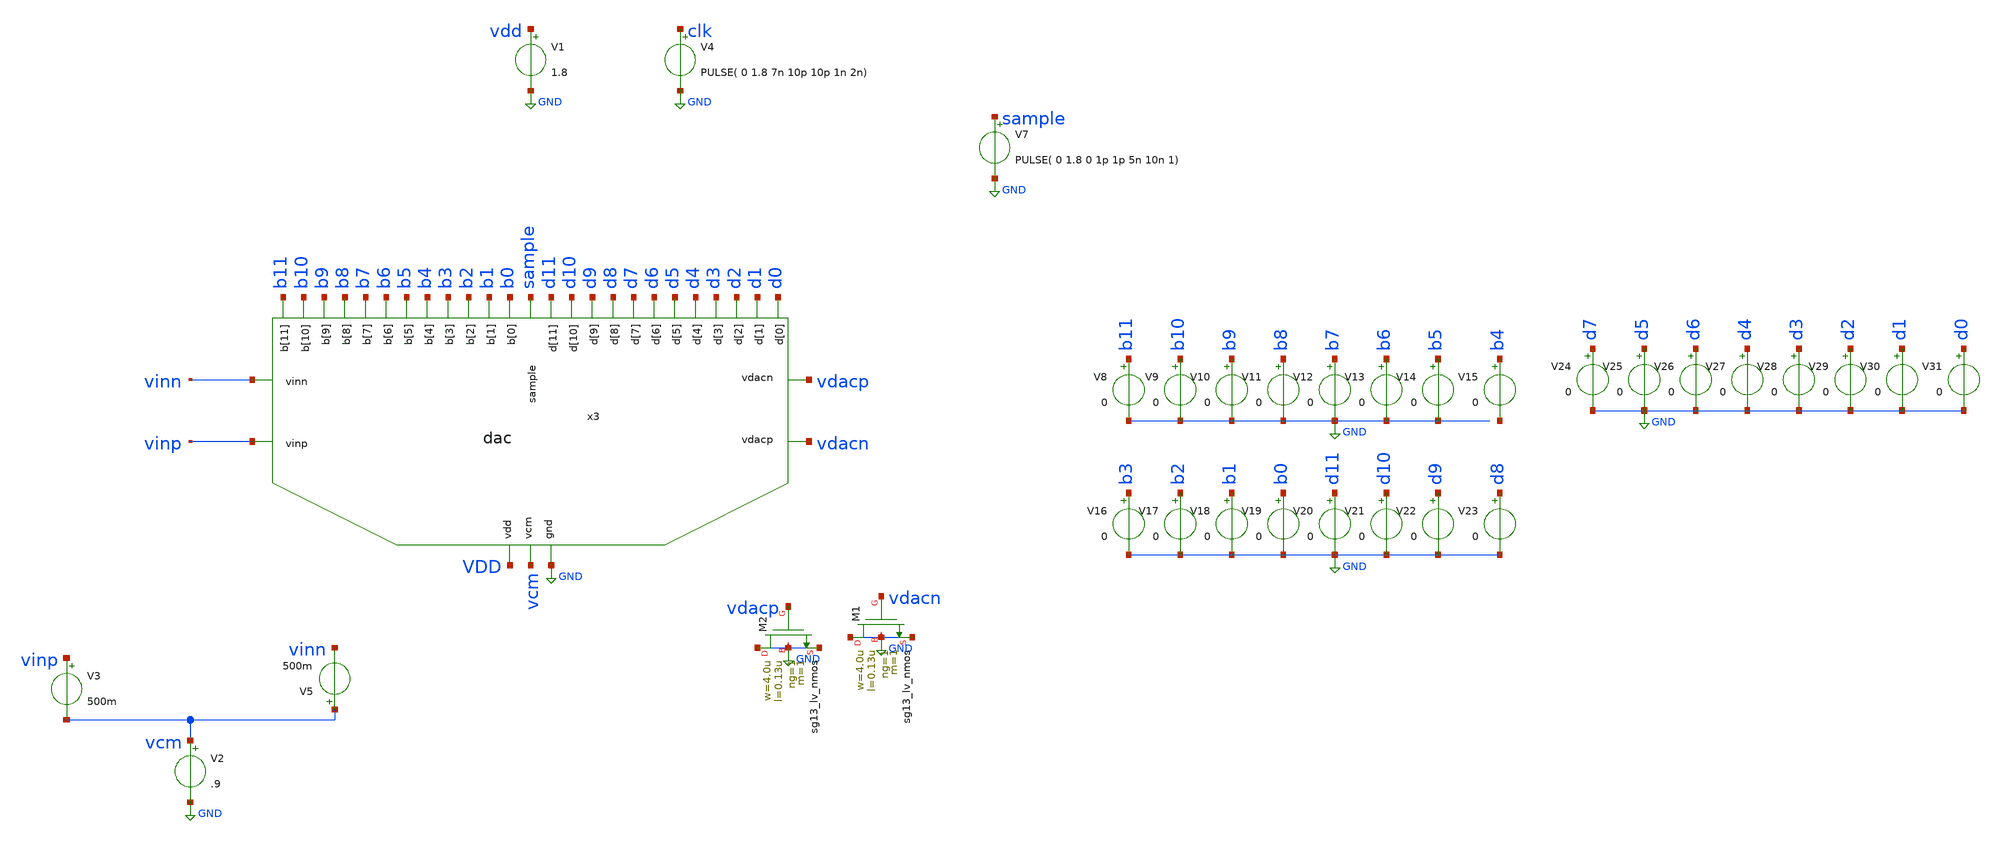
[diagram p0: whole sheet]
** sch_path: xschem/dac_icms_cell_ideall/testbenches/tb_dac_only.sch
* IHP-GmbH/IHP-Open-PDK/ihp-sg13g2/libs.tech/xschem/sg13g2_stdcells/sg13g2_inv_2.sch:
* Copyright 2023 IHP PDK Authors
* Licensed under the Apache License, Version 2.0 (the "License");
**.subckt tb_dac_only
x3 vdacp vcm b9 b7 b0 b11 b3 b4 b2 b1 b8 b6 b5 b10 GND VDD sample vdacn vinp vinn d9 d7 d0 d11 d3 d4
+ d2 d1 d8 d6 d5 d10 dac cu=100f
V1 vdd GND 1.8
V2 vcm GND .9
V3 vinp vcm 500m
V4 clk GND PULSE( 0 1.8 7n 10p 10p 1n 2n)
V7 sample GND PULSE( 0 1.8 0 1p 1p 5n 10n 1)
XM2 GND vdacp GND GND sg13_lv_nmos w=4.0u l=0.13u ng=1 m=1 mm_ok=1
XM1 GND vdacn GND GND sg13_lv_nmos w=4.0u l=0.13u ng=1 m=1 mm_ok=1
V8 b11 GND 0
V9 b10 GND 0
V10 b9 GND 0
V11 b8 GND 0
V12 b7 GND 0
V13 b6 GND 0
V14 b5 GND 0
V15 b4 net1 0
V16 b3 GND 0
V17 b2 GND 0
V18 b1 GND 0
V19 b0 GND 0
V20 d11 GND 0
V21 d10 GND 0
V22 d9 GND 0
V23 d8 GND 0
V24 d7 GND 0
V25 d5 GND 0
V26 d6 GND 0
V27 d4 GND 0
V28 d3 GND 0
V29 d2 GND 0
V30 d1 GND 0
V31 d0 GND 0
V5 vcm vinn 500m
**** begin user architecture code


.param temp=27
.param W_P = 1.0u
.param L_P = 0.13u
.param W_N = 1.0u
.param L_N = 0.13u
.options savecurrents klu method=gear reltol=1e-2 abstol=1e-15 gmin=1e-10
.control

* Transient Analysis
tran 100p 20n

*plot {d0} {d1 + 4} {d2 + 8} {d3 + 12} {d4 + 16} {d5 + 20} {d6 + 24} {d7 + 28} {d8 + 32} {d9 + 36} {d10 + 40}
*+ {d11 + 44}
*plot {b0} {b1 + 4} {b2 + 8} {b3 + 12} {b4 + 16} {b5 + 20} {b6 + 24} {b7 + 28} {b8 + 32} {b9 + 36} {b10 + 40}
*+ {b11 + 44}
*plot {clk} {comp_in + 2} {sample + 4}
plot vdacp vdacn sample
plot {vdacp-vdacn}
plot x3.x14.net1-vdacp x3.x18.vcap-vdacn

.endc




** IHP models
.lib cornerMOSlv.lib mos_tt
.lib cornerMOShv.lib mos_tt
.lib cornerHBT.lib hbt_typ
.lib cornerRES.lib res_typ
.include /foss/pdks/ihp-sg13g2/libs.ref/sg13g2_stdcell/spice/sg13g2_stdcell.spice


**** end user architecture code
**.ends

* expanding   symbol:  dac_icms_cell/dac.sym # of pins=32
** sym_path: xschem/dac_icms_cell_ideal/dac.sym
** sch_path: xschem/dac_icms_cell_ideal/dac.sch
.subckt dac vdacn vcm b9 b7 b0 b11 b3 b4 b2 b1 b8 b6 b5 b10 VSS VDD sample_pin vdacp vinp vinn D9 D7
+ D0 D11 D3 D4 D2 D1 D8 D6 D5 D10  cu=5u
*.ipin D0
*.ipin b0
*.iopin vinp
*.iopin vcm
*.ipin sample_pin
*.iopin vinn
*.iopin vdacp
*.iopin vdacn
*.iopin VSS
*.iopin VDD
*.ipin D1
*.ipin b1
*.ipin D2
*.ipin b2
*.ipin D3
*.ipin b3
*.ipin D4
*.ipin b4
*.ipin D5
*.ipin b5
*.ipin D6
*.ipin b6
*.ipin D7
*.ipin b7
*.ipin D8
*.ipin b8
*.ipin D9
*.ipin b9
*.ipin D10
*.ipin b10
*.ipin D11
*.ipin b11
x14 VDD D0 VSS vdacn b0 vcm vinn a_sample a_sample_n b_sample b_sample_n unit_cell_n W_P=
+ L_P_SPDT=0.13u W_N= L_N_SPDT=0.13u Cu=cu n=32
x18 VDD D0 VSS vdacp b0 vcm vinp a_sample a_sample_n b_sample b_sample_n unit_cell W_P_SPDT=1.0u
+ L_P_SPDT=0.13u W_N_SPDT=1.0u L_N_SPDT=0.13u Cu=cu n=32
C1 vdacp2 vdacn cu m=1
C4 vdacp2 vcm cu m=1
x1 VDD D1 VSS vdacn b1 vcm vinn a_sample a_sample_n b_sample b_sample_n unit_cell_n W_P=
+ L_P_SPDT=0.13u W_N= L_N_SPDT=0.13u Cu=cu n=16
x2 VDD D2 VSS vdacn b2 vcm vinn a_sample a_sample_n b_sample b_sample_n unit_cell_n W_P=
+ L_P_SPDT=0.13u W_N= L_N_SPDT=0.13u Cu=cu n=8
x3 VDD D3 VSS vdacn b3 vcm vinn a_sample a_sample_n b_sample b_sample_n unit_cell_n W_P=
+ L_P_SPDT=0.13u W_N= L_N_SPDT=0.13u Cu=cu n=4
x4 VDD D4 VSS vdacn b4 vcm vinn a_sample a_sample_n b_sample b_sample_n unit_cell_n W_P=
+ L_P_SPDT=0.13u W_N= L_N_SPDT=0.13u Cu=cu n=2
x5 VDD D5 VSS vdacn b5 vcm vinn a_sample a_sample_n b_sample b_sample_n unit_cell_n W_P=
+ L_P_SPDT=0.13u W_N= L_N_SPDT=0.13u Cu=cu n=1
x6 VDD D6 VSS vdacp2 b6 vcm vinn a_sample a_sample_n b_sample b_sample_n unit_cell_n W_P=
+ L_P_SPDT=0.13u W_N= L_N_SPDT=0.13u Cu=cu n=32
x7 VDD D7 VSS vdacp2 b7 vcm vinn a_sample a_sample_n b_sample b_sample_n unit_cell_n W_P=
+ L_P_SPDT=0.13u W_N= L_N_SPDT=0.13u Cu=cu n=16
x8 VDD D8 VSS vdacp2 b8 vcm vinn a_sample a_sample_n b_sample b_sample_n unit_cell_n W_P=
+ L_P_SPDT=0.13u W_N= L_N_SPDT=0.13u Cu=cu n=8
x9 VDD D9 VSS vdacp2 b9 vcm vinn a_sample a_sample_n b_sample b_sample_n unit_cell_n W_P=
+ L_P_SPDT=0.13u W_N= L_N_SPDT=0.13u Cu=cu n=4
x11 VDD D10 VSS vdacp2 b10 vcm vinn a_sample a_sample_n b_sample b_sample_n unit_cell_n W_P=
+ L_P_SPDT=0.13u W_N= L_N_SPDT=0.13u Cu=cu n=2
x12 VDD D11 VSS vdacp2 b11 vcm vinn a_sample a_sample_n b_sample b_sample_n unit_cell_n W_P=
+ L_P_SPDT=0.13u W_N= L_N_SPDT=0.13u Cu=cu n=1
x13 VDD D1 VSS vdacp b1 vcm vinp a_sample a_sample_n b_sample b_sample_n unit_cell W_P_SPDT=1.0u
+ L_P_SPDT=0.13u W_N_SPDT=1.0u L_N_SPDT=0.13u Cu=cu n=16
x15 VDD D2 VSS vdacp b2 vcm vinp a_sample a_sample_n b_sample b_sample_n unit_cell W_P_SPDT=1.0u
+ L_P_SPDT=0.13u W_N_SPDT=1.0u L_N_SPDT=0.13u Cu=cu n=8
x16 VDD D3 VSS vdacp b3 vcm vinp a_sample a_sample_n b_sample b_sample_n unit_cell W_P_SPDT=1.0u
+ L_P_SPDT=0.13u W_N_SPDT=1.0u L_N_SPDT=0.13u Cu=cu n=4
x19 VDD D4 VSS vdacp b4 vcm vinp a_sample a_sample_n b_sample b_sample_n unit_cell W_P_SPDT=1.0u
+ L_P_SPDT=0.13u W_N_SPDT=1.0u L_N_SPDT=0.13u Cu=cu n=2
x20 VDD D5 VSS vdacp b5 vcm vinp a_sample a_sample_n b_sample b_sample_n unit_cell W_P_SPDT=1.0u
+ L_P_SPDT=0.13u W_N_SPDT=1.0u L_N_SPDT=0.13u Cu=cu n=32
C3 vdacn2 vdacp cu m=1
x21 VDD D6 VSS vdacn2 b6 vcm vinp a_sample a_sample_n b_sample b_sample_n unit_cell W_P_SPDT=1.0u
+ L_P_SPDT=0.13u W_N_SPDT=1.0u L_N_SPDT=0.13u Cu=cu n=32
x22 VDD D7 VSS vdacn2 b7 vcm vinp a_sample a_sample_n b_sample b_sample_n unit_cell W_P_SPDT=1.0u
+ L_P_SPDT=0.13u W_N_SPDT=1.0u L_N_SPDT=0.13u Cu=cu n=16
x23 VDD D8 VSS vdacn2 b8 vcm vinp a_sample a_sample_n b_sample b_sample_n unit_cell W_P_SPDT=1.0u
+ L_P_SPDT=0.13u W_N_SPDT=1.0u L_N_SPDT=0.13u Cu=cu n=8
x24 VDD D9 VSS vdacn2 b9 vcm vinp a_sample a_sample_n b_sample b_sample_n unit_cell W_P_SPDT=1.0u
+ L_P_SPDT=0.13u W_N_SPDT=1.0u L_N_SPDT=0.13u Cu=cu n=4
x25 VDD D10 VSS vdacn2 b10 vcm vinp a_sample a_sample_n b_sample b_sample_n unit_cell W_P_SPDT=1.0u
+ L_P_SPDT=0.13u W_N_SPDT=1.0u L_N_SPDT=0.13u Cu=cu n=2
x26 VDD D11 VSS vdacn2 b11 vcm vinp a_sample a_sample_n b_sample b_sample_n unit_cell W_P_SPDT=1.0u
+ L_P_SPDT=0.13u W_N_SPDT=1.0u L_N_SPDT=0.13u Cu=cu n=32
C5 vcm vdacn2 cu m=1
x27 VDD b_n_ctrl net3 VSS inverter_lv W_P=1.0u L_P=0.13u W_N=1.0u L_N=0.13u N_C=1
x28 VDD net3 b_sample_n VSS inverter_lv W_P=10.0u L_P=0.13u W_N=10.0u L_N=0.13u N_C=1
x29 VDD b_ctrl net4 VSS inverter_lv W_P=1.0u L_P=0.13u W_N=1.0u L_N=0.13u N_C=1
x31 VDD net4 b_sample VSS inverter_lv W_P=10.0u L_P=0.13u W_N=10.0u L_N=0.13u N_C=1
x32 VDD a_n_ctrl net5 VSS inverter_lv W_P=1.0u L_P=0.13u W_N=1.0u L_N=0.13u N_C=1
x33 VDD net5 a_sample_n VSS inverter_lv W_P=20.0u L_P=0.13u W_N=10.0u L_N=0.13u N_C=1
x35 VDD a_ctrl net6 VSS inverter_lv W_P=1.0u L_P=0.13u W_N=1.0u L_N=0.13u N_C=1
x36 VDD net6 a_sample VSS inverter_lv W_P=20.0u L_P=0.13u W_N=10.0u L_N=0.13u N_C=1
x38 b_ctrl sample_pin net2 VDD VSS sg13g2_nor2_2
x39 a_n_ctrl net1 sample_pin VDD VSS sg13g2_nand2_2
x40 b_n_ctrl b_ctrl VDD VSS sg13g2_inv_2
x41 a_ctrl a_n_ctrl VDD VSS sg13g2_inv_2
x42 net2 a_sample_n net7 VDD VSS sg13g2_nand2_2
x43 net1 b_sample net8 VDD VSS sg13g2_nor2_2
x44 net7 a_sample VDD VSS sg13g2_inv_1
x45 net8 b_sample_n VDD VSS sg13g2_inv_1
.ends


* expanding   symbol:  dac_icms_cell/unit_cell_n.sym # of pins=11
** sym_path: xschem/dac_icms_cell/unit_cell_n.sym
** sch_path: xschem/dac_icms_cell/unit_cell_n.sch
.subckt unit_cell_n VDD d VSS v_top bit v_cm v_in a_sample a_sample_n b_sample b_sample_n
+  W_P_SPDT=1.0u L_P_SPDT=0.13u W_N_SPDT=1.0u L_N_SPDT=0.13u Cu=8f n=1
*.iopin VSS
*.iopin v_in
*.iopin VDD
*.ipin d
*.ipin bit
*.iopin v_top
*.iopin v_cm
*.ipin a_sample
*.ipin a_sample_n
*.ipin b_sample
*.ipin b_sample_n
x1 VDD d VSS net1 bit v_cm v_in b_sample_n b_sample dac_switch_n W_P_TG=3.0u L_P_TG=0.13u
+ W_N_TG=1.0u L_N_TG=0.13u n=n
C1 net1 v_top Cu m=n
x2 VDD a_sample VSS v_cm v_top a_sample_n transmission_gate_lv_w_dummy W_P=W_P_SPDT L_P=L_P_SPDT
+ W_N=W_N_SPDT L_N=L_N_SPDT W_P_D=1.0u L_P_D=0.13u W_N_D=1.0u L_N_D=0.13u n=n
.ends


* expanding   symbol:  dac_icms_cell/unit_cell.sym # of pins=11
** sym_path: xschem/dac_icms_cell/unit_cell.sym
** sch_path: xschem/dac_icms_cell/unit_cell.sch
.subckt unit_cell VDD d VSS v_top bit v_cm v_in a_sample a_sample_n b_sample b_sample_n
+  W_P_SPDT=1.0u L_P_SPDT=0.13u W_N_SPDT=1.0u L_N_SPDT=0.13u Cu=8f n=1
*.iopin VSS
*.iopin v_in
*.iopin VDD
*.ipin d
*.ipin bit
*.iopin v_top
*.iopin v_cm
*.ipin a_sample_n
*.ipin a_sample
*.ipin b_sample
*.ipin b_sample_n
x1 VDD d VSS net1 bit v_cm v_in b_sample_n b_sample dac_switch W_P=W_P_SPDT L_P_TG=0.13u
+ W_N=W_N_SPDT L_N_TG=0.13u n=n
C1 net1 v_top Cu m=n
x2 VDD a_sample_n VSS v_cm v_top a_sample transmission_gate_lv_w_dummy W_P=W_P_SPDT L_P=L_P_SPDT
+ W_N=W_N_SPDT L_N=L_N_SPDT W_P_D=1.0u L_P_D=0.13u W_N_D=1.0u L_N_D=0.13u n=n
.ends


* expanding   symbol:  inverter/inverter_lv.sym # of pins=4
** sym_path: xschem/inverter/inverter_lv.sym
** sch_path: xschem/inverter/inverter_lv.sch
.subckt inverter_lv VDD vin vout VSS  W_P=3.0u L_P=0.13u W_N=1.0u L_N=0.13u N_C=1
*.ipin vin
*.iopin VDD
*.iopin VSS
*.opin vout
XM1 vout vin VDD VDD sg13_lv_pmos w=W_P l=L_P ng=1 m={N_C} mm_ok=1
XM2 vout vin VSS VSS sg13_lv_nmos w=W_N l=L_N ng=1 m={N_C} mm_ok=1
.ends


* expanding   symbol:  sg13g2_stdcells/sg13g2_nor2_2.sym # of pins=3
** sym_path: sg13g2_stdcells/sg13g2_nor2_2.sym
** sch_path: sg13g2_stdcells/sg13g2_nor2_2.sch
.subckt sg13g2_nor2_2 Y A B VDD VSS
*.opin Y
*.ipin B
*.ipin A
*.iopin VDD
*.iopin VSS
XM1 Y A VSS VSS sg13_lv_nmos w=1.48u l=130.00n ng=2 m=1 mm_ok=1
XM2 Y B VSS VSS sg13_lv_nmos w=1.48u l=130.00n ng=2 m=1 mm_ok=1
XM3 net1 A VDD VDD sg13_lv_pmos w=2.24u l=130.00n ng=2 m=1 mm_ok=1
XM4 Y B net1 VDD sg13_lv_pmos w=2.24u l=130.00n ng=2 m=1 mm_ok=1
.ends


* expanding   symbol:  sg13g2_stdcells/sg13g2_nand2_2.sym # of pins=3
** sym_path: sg13g2_stdcells/sg13g2_nand2_2.sym
** sch_path: sg13g2_stdcells/sg13g2_nand2_2.sch
.subckt sg13g2_nand2_2 Y A B VDD VSS
*.iopin VDD
*.iopin VSS
*.opin Y
*.ipin B
*.ipin A
XM1 Y A net1 VSS sg13_lv_nmos w=1.44u l=130.00n ng=2 m=1 mm_ok=1
XM2 net1 B VSS VSS sg13_lv_nmos w=1.44u l=130.00n ng=2 m=1 mm_ok=1
XM3 Y A VDD VDD sg13_lv_pmos w=2.24u l=130.00n ng=2 m=1 mm_ok=1
XM4 Y B VDD VDD sg13_lv_pmos w=2.24u l=130.00n ng=2 m=1 mm_ok=1
.ends


* expanding   symbol:  sg13g2_stdcells/sg13g2_inv_2.sym # of pins=2
** sym_path: sg13g2_stdcells/sg13g2_inv_2.sym
** sch_path: sg13g2_stdcells/sg13g2_inv_2.sch
.subckt sg13g2_inv_2 Y A VDD VSS
*.opin Y
*.ipin A
*.iopin VDD
*.iopin VSS
XM1 Y A VSS VSS sg13_lv_nmos w=1.48u l=130.00n ng=2 m=1 mm_ok=1
XM2 Y A VDD VDD sg13_lv_pmos w=2.24u l=130.00n ng=2 m=1 mm_ok=1
.ends


* expanding   symbol:  sg13g2_stdcells/sg13g2_inv_1.sym # of pins=2
** sym_path: sg13g2_stdcells/sg13g2_inv_1.sym
** sch_path: sg13g2_stdcells/sg13g2_inv_1.sch
.subckt sg13g2_inv_1 Y A VDD VSS
*.opin Y
*.ipin A
*.iopin VDD
*.iopin VSS
XM1 Y A VSS VSS sg13_lv_nmos w=740.00n l=130.00n ng=1 m=1 mm_ok=1
XM2 Y A VDD VDD sg13_lv_pmos w=1.12u l=130.00n ng=1 m=1 mm_ok=1
.ends


* expanding   symbol:  dac_icms_cell/dac_switch_n.sym # of pins=9
** sym_path: xschem/dac_icms_cell/dac_switch_n.sym
** sch_path: xschem/dac_icms_cell/dac_switch_n.sch
.subckt dac_switch_n VDD d VSS v_cap bit v_cm v_in sample sample_n  W_P_TG=3.0u L_P_TG=0.13u
+ W_N_TG=1.0u L_N_TG=0.13u n=1
*.iopin v_in
*.iopin v_cap
*.iopin VDD
*.iopin VSS
*.ipin d
*.iopin v_cm
*.ipin bit
*.ipin sample
*.ipin sample_n
x8 VDD d d_n VSS inverter_lv W_P=W_P_TG L_P=L_P_TG W_N=W_N_TG L_N=L_N_TG N_C=1
XM1 v_cap net3 VSS VSS sg13_lv_nmos w=1u l=0.2u ng=1 m=n mm_ok=1
XM3 v_cap net4 VDD VDD sg13_lv_pmos w=1.2u l=0.13u ng=1 m=n mm_ok=1
x2 VDD net2 VSS v_cap v_cm net1 transmission_gate_lv_w_dummy W_P=W_P_TG L_P=L_P_TG W_N=W_N_TG
+ L_N=L_N_TG W_P_D=1.0u L_P_D=0.13u W_N_D=1.0u L_N_D=0.13u n=n
x1 VDD sample VSS v_cap v_in sample_n transmission_gate_lv_w_dummy W_P=W_P_TG L_P=L_P_TG W_N=W_N_TG
+ L_N=L_N_TG W_P_D=1.0u L_P_D=0.13u W_N_D=1.0u L_N_D=0.13u n=n
x23 net5 bit d VDD VSS sg13g2_nand2_1
x46 net6 net9 d VDD VSS sg13g2_and2_1
x4 VDD net5 net4 VSS buffer_lv W_P_INV=3.0u L_P_INV=0.13u W_N_INV=1.0u L_N_INV=0.13u
x5 VDD net6 net3 VSS buffer_lv W_P_INV=3.0u L_P_INV=0.13u W_N_INV=1.0u L_N_INV=0.13u
x3 net7 d sample VDD VSS sg13g2_nor2_1
x6 net8 d sample VDD VSS sg13g2_or2_1
x7 VDD net7 net2 VSS buffer_lv W_P_INV=3.0u L_P_INV=0.13u W_N_INV=1.0u L_N_INV=0.13u
x9 VDD net8 net1 VSS buffer_lv W_P_INV=3.0u L_P_INV=0.13u W_N_INV=1.0u L_N_INV=0.13u
x32 net9 bit VDD VSS sg13g2_inv_1
.ends


* expanding   symbol:  transmission_gate/transmission_gate_lv_w_dummy.sym # of pins=6
** sym_path: xschem/transmission_gate/transmission_gate_lv_w_dummy.sym
** sch_path: xschem/transmission_gate/transmission_gate_lv_w_dummy.sch
.subckt transmission_gate_lv_w_dummy VDD di_tg_ctrl VSS v_b v_a di_tg_ctrl_n  W_P=2.0u L_P=0.13u
+ W_N=2.0u L_N=0.13u W_P_D=1.0u L_P_D=0.13u W_N_D=1.0u L_N_D=0.13u n=1
*.iopin v_a
*.iopin v_b
*.iopin VDD
*.iopin VSS
*.ipin di_tg_ctrl
*.ipin di_tg_ctrl_n
XM1 v_a di_tg_ctrl v_b VSS sg13_lv_nmos w=W_N l=L_N ng=1 m=n mm_ok=1
XM2 v_a di_tg_ctrl_n v_b VDD sg13_lv_pmos w=W_P l=L_P ng=1 m=n mm_ok=1
XMdummy2 v_b di_tg_ctrl v_b VDD sg13_lv_pmos w=W_P l=L_P ng=1 m={n/2} mm_ok=1
XMdummy1 v_b di_tg_ctrl_n v_b VSS sg13_lv_nmos w=W_N l=L_N ng=1 m={n/2} mm_ok=1
.ends


* expanding   symbol:  dac_icms_cell/dac_switch.sym # of pins=9
** sym_path: xschem/dac_icms_cell/dac_switch.sym
** sch_path: xschem/dac_icms_cell/dac_switch.sch
.subckt dac_switch VDD d VSS v_cap bit v_cm v_in sample sample_n  W_P_TG=3.0u L_P_TG=0.13u
+ W_N_TG=1.0u L_N_TG=0.13u n=1
*.iopin v_in
*.iopin v_cap
*.iopin VDD
*.iopin VSS
*.ipin d
*.ipin bit
*.ipin sample
*.ipin sample_n
*.iopin v_cm
x8 VDD d d_n VSS inverter_lv W_P=W_P_TG L_P=L_P_TG W_N=W_N_TG L_N=L_N_TG N_C=1
XM1 v_cap net1 VSS VSS sg13_lv_nmos w=1u l=0.13u ng=1 m=n mm_ok=1
XM3 v_cap net2 VDD VDD sg13_lv_pmos w=1.2u l=0.2u ng=1 m=n mm_ok=1
x1 VDD sample VSS v_cap v_in sample_n transmission_gate_lv_w_dummy W_P=W_P_TG L_P=L_P_TG W_N=W_N_TG
+ L_N=L_N_TG W_P_D=1.0u L_P_D=0.13u W_N_D=1.0u L_N_D=0.13u n=n
x23 net3 net9 d VDD VSS sg13g2_nand2_1
x46 net4 bit d VDD VSS sg13g2_and2_1
x4 VDD net3 net2 VSS buffer_lv W_P_INV=3.0u L_P_INV=0.13u W_N_INV=1.0u L_N_INV=0.13u
x5 VDD net4 net1 VSS buffer_lv W_P_INV=3.0u L_P_INV=0.13u W_N_INV=1.0u L_N_INV=0.13u
x32 net9 bit VDD VSS sg13g2_inv_1
x3 VDD net6 VSS v_cap v_cm net5 transmission_gate_lv_w_dummy W_P=W_P_TG L_P=L_P_TG W_N=W_N_TG
+ L_N=L_N_TG W_P_D=1.0u L_P_D=0.13u W_N_D=1.0u L_N_D=0.13u n=n
x6 net7 d sample VDD VSS sg13g2_nor2_1
x7 net8 d sample VDD VSS sg13g2_or2_1
x9 VDD net7 net6 VSS buffer_lv W_P_INV=3.0u L_P_INV=0.13u W_N_INV=1.0u L_N_INV=0.13u
x10 VDD net8 net5 VSS buffer_lv W_P_INV=3.0u L_P_INV=0.13u W_N_INV=1.0u L_N_INV=0.13u
.ends


* expanding   symbol:  sg13g2_stdcells/sg13g2_nand2_1.sym # of pins=3
** sym_path: sg13g2_stdcells/sg13g2_nand2_1.sym
** sch_path: sg13g2_stdcells/sg13g2_nand2_1.sch
.subckt sg13g2_nand2_1 Y A B VDD VSS
*.iopin VDD
*.iopin VSS
*.ipin A
*.ipin B
*.opin Y
XM1 Y A net1 VSS sg13_lv_nmos w=740.00n l=130.00n ng=1 m=1 mm_ok=1
XM2 net1 B VSS VSS sg13_lv_nmos w=740.00n l=130.00n ng=1 m=1 mm_ok=1
XM3 Y A VDD VDD sg13_lv_pmos w=1.12u l=130.00n ng=1 m=1 mm_ok=1
XM4 Y B VDD VDD sg13_lv_pmos w=1.12u l=130.00n ng=1 m=1 mm_ok=1
.ends


* expanding   symbol:  sg13g2_stdcells/sg13g2_and2_1.sym # of pins=3
** sym_path: sg13g2_stdcells/sg13g2_and2_1.sym
** sch_path: sg13g2_stdcells/sg13g2_and2_1.sch
.subckt sg13g2_and2_1 X A B VDD VSS
*.ipin A
*.ipin B
*.opin X
*.iopin VDD
*.iopin VSS
XM1 net1 A net2 VSS sg13_lv_nmos w=640.00n l=130.00n ng=1 m=1 mm_ok=1
XM2 net2 B VSS VSS sg13_lv_nmos w=640.00n l=130.00n ng=1 m=1 mm_ok=1
XM3 X net1 VSS VSS sg13_lv_nmos w=740.00n l=130.00n ng=1 m=1 mm_ok=1
XM4 net1 B VDD VDD sg13_lv_pmos w=840.00n l=130.00n ng=1 m=1 mm_ok=1
XM5 net1 A VDD VDD sg13_lv_pmos w=840.00n l=130.00n ng=1 m=1 mm_ok=1
XM6 X net1 VDD VDD sg13_lv_pmos w=1.12u l=130.00n ng=1 m=1 mm_ok=1
.ends


* expanding   symbol:  buffer/buffer_lv.sym # of pins=4
** sym_path: buffer/buffer_lv.sym
** sch_path: buffer/buffer_lv.sch
.subckt buffer_lv VDD vin vout VSS  W_P_INV=3.0u L_P_INV=0.13u W_N_INV=1.0u L_N_INV=0.13u
*.ipin vin
*.iopin VDD
*.iopin VSS
*.opin vout
x1 VDD vin net1 VSS inverter_lv W_P=W_P_INV L_P=L_P_INV W_N=W_N_INV L_N=L_N_INV N_C=1
x2 VDD net1 vout VSS inverter_lv W_P=W_P_INV L_P=L_P_INV W_N=W_N_INV L_N=L_N_INV N_C=1
.ends


* expanding   symbol:  sg13g2_stdcells/sg13g2_nor2_1.sym # of pins=3
** sym_path: sg13g2_stdcells/sg13g2_nor2_1.sym
** sch_path: sg13g2_stdcells/sg13g2_nor2_1.sch
.subckt sg13g2_nor2_1 Y A B VDD VSS
*.opin Y
*.ipin B
*.ipin A
*.iopin VDD
*.iopin VSS
XM1 Y A VSS VSS sg13_lv_nmos w=740.00n l=130.00n ng=1 m=1 mm_ok=1
XM2 Y B VSS VSS sg13_lv_nmos w=740.00n l=130.00n ng=1 m=1 mm_ok=1
XM3 net1 A VDD VDD sg13_lv_pmos w=1.12u l=130.00n ng=1 m=1 mm_ok=1
XM4 Y B net1 VDD sg13_lv_pmos w=1.12u l=130.00n ng=1 m=1 mm_ok=1
.ends


* expanding   symbol:  sg13g2_stdcells/sg13g2_or2_1.sym # of pins=3
** sym_path: sg13g2_stdcells/sg13g2_or2_1.sym
** sch_path: sg13g2_stdcells/sg13g2_or2_1.sch
.subckt sg13g2_or2_1 X A B VDD VSS
*.opin X
*.ipin B
*.ipin A
*.iopin VDD
*.iopin VSS
XM1 net1 B VSS VSS sg13_lv_nmos w=550.00n l=130.00n ng=1 m=1 mm_ok=1
XM2 net1 A VSS VSS sg13_lv_nmos w=550.00n l=130.00n ng=1 m=1 mm_ok=1
XM3 X net1 VSS VSS sg13_lv_nmos w=740.00n l=130.00n ng=1 m=1 mm_ok=1
XM4 net2 A VDD VDD sg13_lv_pmos w=840.00n l=130.00n ng=1 m=1 mm_ok=1
XM5 net1 B net2 VDD sg13_lv_pmos w=840.00n l=130.00n ng=1 m=1 mm_ok=1
XM6 X net1 VDD VDD sg13_lv_pmos w=1.12u l=130.00n ng=1 m=1 mm_ok=1
.ends

.GLOBAL GND
.end
